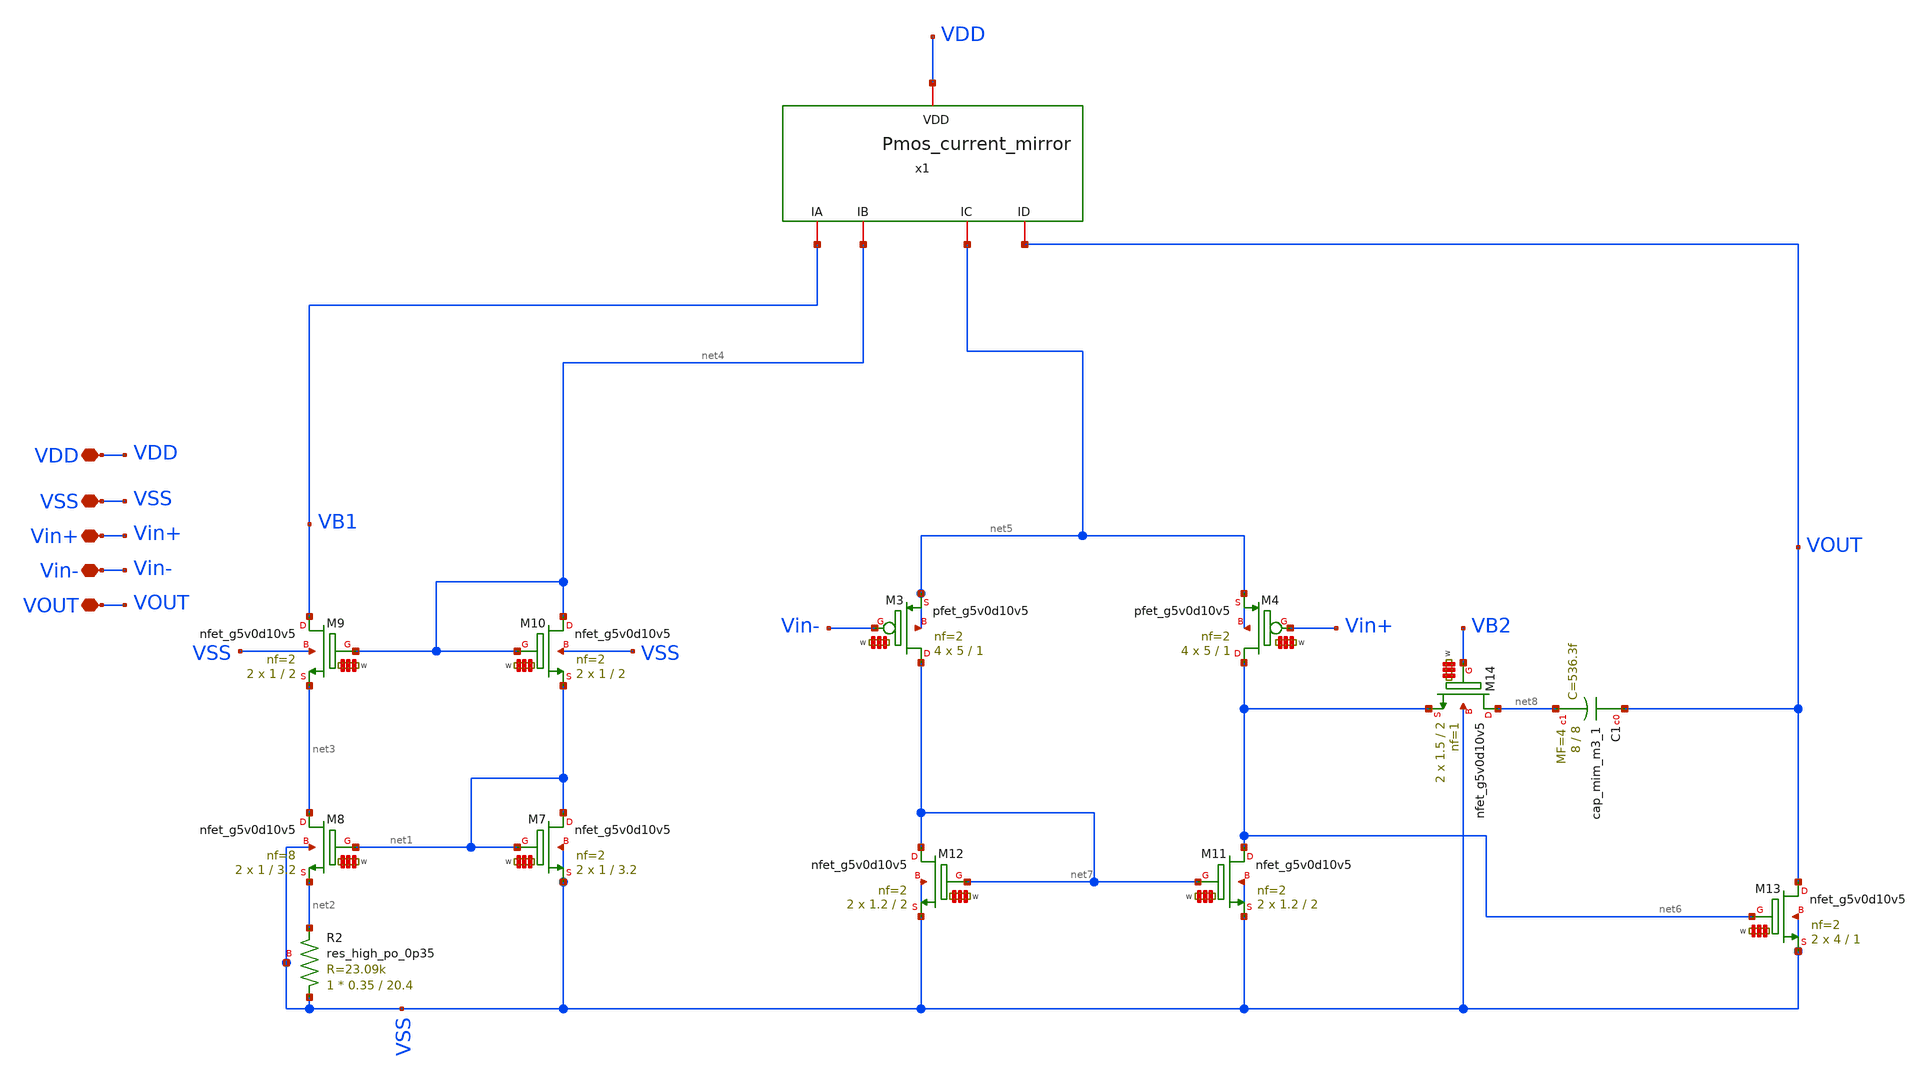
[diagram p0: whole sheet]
** sch_path: my_ip/LIB/Sky130A/Learning/Design_of_Two-Stage_CMOS_Operational_Amplifier_for_Fluorescence_Signal_Processing_5V/A001.sch
**.subckt A001 VDD VSS Vin+ Vin- VOUT
*.iopin VDD
*.iopin VSS
*.iopin Vin+
*.iopin Vin-
*.iopin VOUT
XR2 VSS net2 VSS sky130_fd_pr__res_high_po_0p35 L=20.4 mult=1 m=1
XM7 net1 net1 VSS VSS sky130_fd_pr__nfet_g5v0d10v5 L=3.2 W='1 * 2 ' nf=2 ad='int((nf+1)/2) * W / nf * 0.29'
+ as='int((nf+2)/2) * W / nf * 0.29' pd='2*int((nf+1)/2) * (W / nf + 0.29)' ps='2*int((nf+2)/2) * (W / nf + 0.29)'
+ nrd='0.29 / W ' nrs='0.29 / W ' sa=0 sb=0 sd=0 mult=2 m=2
XM8 net3 net1 net2 VSS sky130_fd_pr__nfet_g5v0d10v5 L=3.2 W='1 * 8 ' nf=8 ad='int((nf+1)/2) * W / nf * 0.29'
+ as='int((nf+2)/2) * W / nf * 0.29' pd='2*int((nf+1)/2) * (W / nf + 0.29)' ps='2*int((nf+2)/2) * (W / nf + 0.29)'
+ nrd='0.29 / W ' nrs='0.29 / W ' sa=0 sb=0 sd=0 mult=2 m=2
XM9 VB1 net4 net3 VSS sky130_fd_pr__nfet_g5v0d10v5 L=2 W='1 * 2 ' nf=2 ad='int((nf+1)/2) * W / nf * 0.29'
+ as='int((nf+2)/2) * W / nf * 0.29' pd='2*int((nf+1)/2) * (W / nf + 0.29)' ps='2*int((nf+2)/2) * (W / nf + 0.29)'
+ nrd='0.29 / W ' nrs='0.29 / W ' sa=0 sb=0 sd=0 mult=2 m=2
XM10 net4 net4 net1 VSS sky130_fd_pr__nfet_g5v0d10v5 L=2 W='1 * 2 ' nf=2 ad='int((nf+1)/2) * W / nf * 0.29'
+ as='int((nf+2)/2) * W / nf * 0.29' pd='2*int((nf+1)/2) * (W / nf + 0.29)' ps='2*int((nf+2)/2) * (W / nf + 0.29)'
+ nrd='0.29 / W ' nrs='0.29 / W ' sa=0 sb=0 sd=0 mult=2 m=2
XM3 net7 Vin- net5 net5 sky130_fd_pr__pfet_g5v0d10v5 L=1 W='5 * 2 ' nf=2 ad='int((2 + 1)/2) * 5 * 0.29'
+ as='int((2 + 2)/2) * 5 * 0.29' pd='2*int((2 + 1)/2) * (5 + 0.29)' ps='2*int((2 + 2)/2) * (5 + 0.29)'
+ nrd='0.29 / 5 / 2 ' nrs='0.29 / 5 / 2 ' sa=0 sb=0 sd=0 mult=4 m=4
XM4 net6 Vin+ net5 net5 sky130_fd_pr__pfet_g5v0d10v5 L=1 W='5 * 2 ' nf=2 ad='int((2 + 1)/2) * 5 * 0.29'
+ as='int((2 + 2)/2) * 5 * 0.29' pd='2*int((2 + 1)/2) * (5 + 0.29)' ps='2*int((2 + 2)/2) * (5 + 0.29)'
+ nrd='0.29 / 5 / 2 ' nrs='0.29 / 5 / 2 ' sa=0 sb=0 sd=0 mult=4 m=4
XM11 net6 net7 VSS VSS sky130_fd_pr__nfet_g5v0d10v5 L=2 W='1.2 * 2 ' nf=2 ad='int((nf+1)/2) * W / nf * 0.29'
+ as='int((nf+2)/2) * W / nf * 0.29' pd='2*int((nf+1)/2) * (W / nf + 0.29)' ps='2*int((nf+2)/2) * (W / nf + 0.29)'
+ nrd='0.29 / W ' nrs='0.29 / W ' sa=0 sb=0 sd=0 mult=2 m=2
XM12 net7 net7 VSS VSS sky130_fd_pr__nfet_g5v0d10v5 L=2 W='1.2 * 2 ' nf=2 ad='int((nf+1)/2) * W / nf * 0.29'
+ as='int((nf+2)/2) * W / nf * 0.29' pd='2*int((nf+1)/2) * (W / nf + 0.29)' ps='2*int((nf+2)/2) * (W / nf + 0.29)'
+ nrd='0.29 / W ' nrs='0.29 / W ' sa=0 sb=0 sd=0 mult=2 m=2
XM13 VOUT net6 VSS VSS sky130_fd_pr__nfet_g5v0d10v5 L=1 W='4 * 2 ' nf=2 ad='int((nf+1)/2) * W / nf * 0.29'
+ as='int((nf+2)/2) * W / nf * 0.29' pd='2*int((nf+1)/2) * (W / nf + 0.29)' ps='2*int((nf+2)/2) * (W / nf + 0.29)'
+ nrd='0.29 / W ' nrs='0.29 / W ' sa=0 sb=0 sd=0 mult=2 m=2
XM14 net8 VB2 net6 VSS sky130_fd_pr__nfet_g5v0d10v5 L=2 W='1.5 * 1 ' nf=1 ad='int((nf+1)/2) * W / nf * 0.29'
+ as='int((nf+2)/2) * W / nf * 0.29' pd='2*int((nf+1)/2) * (W / nf + 0.29)' ps='2*int((nf+2)/2) * (W / nf + 0.29)'
+ nrd='0.29 / W ' nrs='0.29 / W ' sa=0 sb=0 sd=0 mult=2 m=2
XC1 VOUT net8 sky130_fd_pr__cap_mim_m3_1 W=8 L=8 MF=4 m=4
x1 VDD VB1 net4 net5 VOUT Pmos_current_mirror
**.ends

* expanding   symbol:
*+  Sky130A/Learning/Design_of_Two-Stage_CMOS_Operational_Amplifier_for_Fluorescence_Signal_Processing_5V/Pmos_current_mirror.sym # of pins=5
** sym_path: Learning/single_ended_amplifiers/Design_and_Analysis_of_Two-Stage_CMOS_Operational_Amplifier_for_Fluorescence_Signal_Processing_sky130_5V/klayout_layout/Pmos_current_mirror.sym
** sch_path: Learning/single_ended_amplifiers/Design_and_Analysis_of_Two-Stage_CMOS_Operational_Amplifier_for_Fluorescence_Signal_Processing_sky130_5V/klayout_layout/Pmos_current_mirror.sch
.subckt Pmos_current_mirror VDD IA IB IC ID
*.iopin VDD
*.iopin IA
*.iopin IB
*.iopin IC
*.iopin ID
XM2 IB IA VDD VDD sky130_fd_pr__pfet_g5v0d10v5 L=2.2 W='1 * 2 ' nf=2 ad='int((2 + 1)/2) * 1 * 0.29' as='int((2 + 2)/2) * 1 * 0.29'
+ pd='2*int((2 + 1)/2) * (1 + 0.29)' ps='2*int((2 + 2)/2) * (1 + 0.29)' nrd='0.29 / 1 / 2 ' nrs='0.29 / 1 / 2 '
+ sa=0 sb=0 sd=0 mult=2 m=2
XM3 IA IA VDD VDD sky130_fd_pr__pfet_g5v0d10v5 L=2.2 W='1 * 2 ' nf=2 ad='int((2 + 1)/2) * 1 * 0.29' as='int((2 + 2)/2) * 1 * 0.29'
+ pd='2*int((2 + 1)/2) * (1 + 0.29)' ps='2*int((2 + 2)/2) * (1 + 0.29)' nrd='0.29 / 1 / 2 ' nrs='0.29 / 1 / 2 '
+ sa=0 sb=0 sd=0 mult=2 m=2
XM4 IC IA VDD VDD sky130_fd_pr__pfet_g5v0d10v5 L=2.2 W='1 * 2 ' nf=2 ad='int((2 + 1)/2) * 1 * 0.29' as='int((2 + 2)/2) * 1 * 0.29'
+ pd='2*int((2 + 1)/2) * (1 + 0.29)' ps='2*int((2 + 2)/2) * (1 + 0.29)' nrd='0.29 / 1 / 2 ' nrs='0.29 / 1 / 2 '
+ sa=0 sb=0 sd=0 mult=8 m=8
XM7 ID IA VDD VDD sky130_fd_pr__pfet_g5v0d10v5 L=2.2 W='1 * 2 ' nf=2 ad='int((2 + 1)/2) * 1 * 0.29' as='int((2 + 2)/2) * 1 * 0.29'
+ pd='2*int((2 + 1)/2) * (1 + 0.29)' ps='2*int((2 + 2)/2) * (1 + 0.29)' nrd='0.29 / 1 / 2 ' nrs='0.29 / 1 / 2 '
+ sa=0 sb=0 sd=0 mult=16 m=16
XM1 IA VDD VDD VDD sky130_fd_pr__pfet_g5v0d10v5 L=2.2 W='1 * 1 ' nf=1 ad='int((1 + 1)/2) * 1 * 0.29'
+ as='int((1 + 2)/2) * 1 * 0.29' pd='2*int((1 + 1)/2) * (1 + 0.29)' ps='2*int((1 + 2)/2) * (1 + 0.29)'
+ nrd='0.29 / 1 / 1 ' nrs='0.29 / 1 / 1 ' sa=0 sb=0 sd=0 mult=4 m=4
XM5 VDD VDD VDD VDD sky130_fd_pr__pfet_g5v0d10v5 L=2.2 W='1 * 1 ' nf=1 ad='int((1 + 1)/2) * 1 * 0.29'
+ as='int((1 + 2)/2) * 1 * 0.29' pd='2*int((1 + 1)/2) * (1 + 0.29)' ps='2*int((1 + 2)/2) * (1 + 0.29)'
+ nrd='0.29 / 1 / 1 ' nrs='0.29 / 1 / 1 ' sa=0 sb=0 sd=0 mult=2 m=2
.ends

.end
